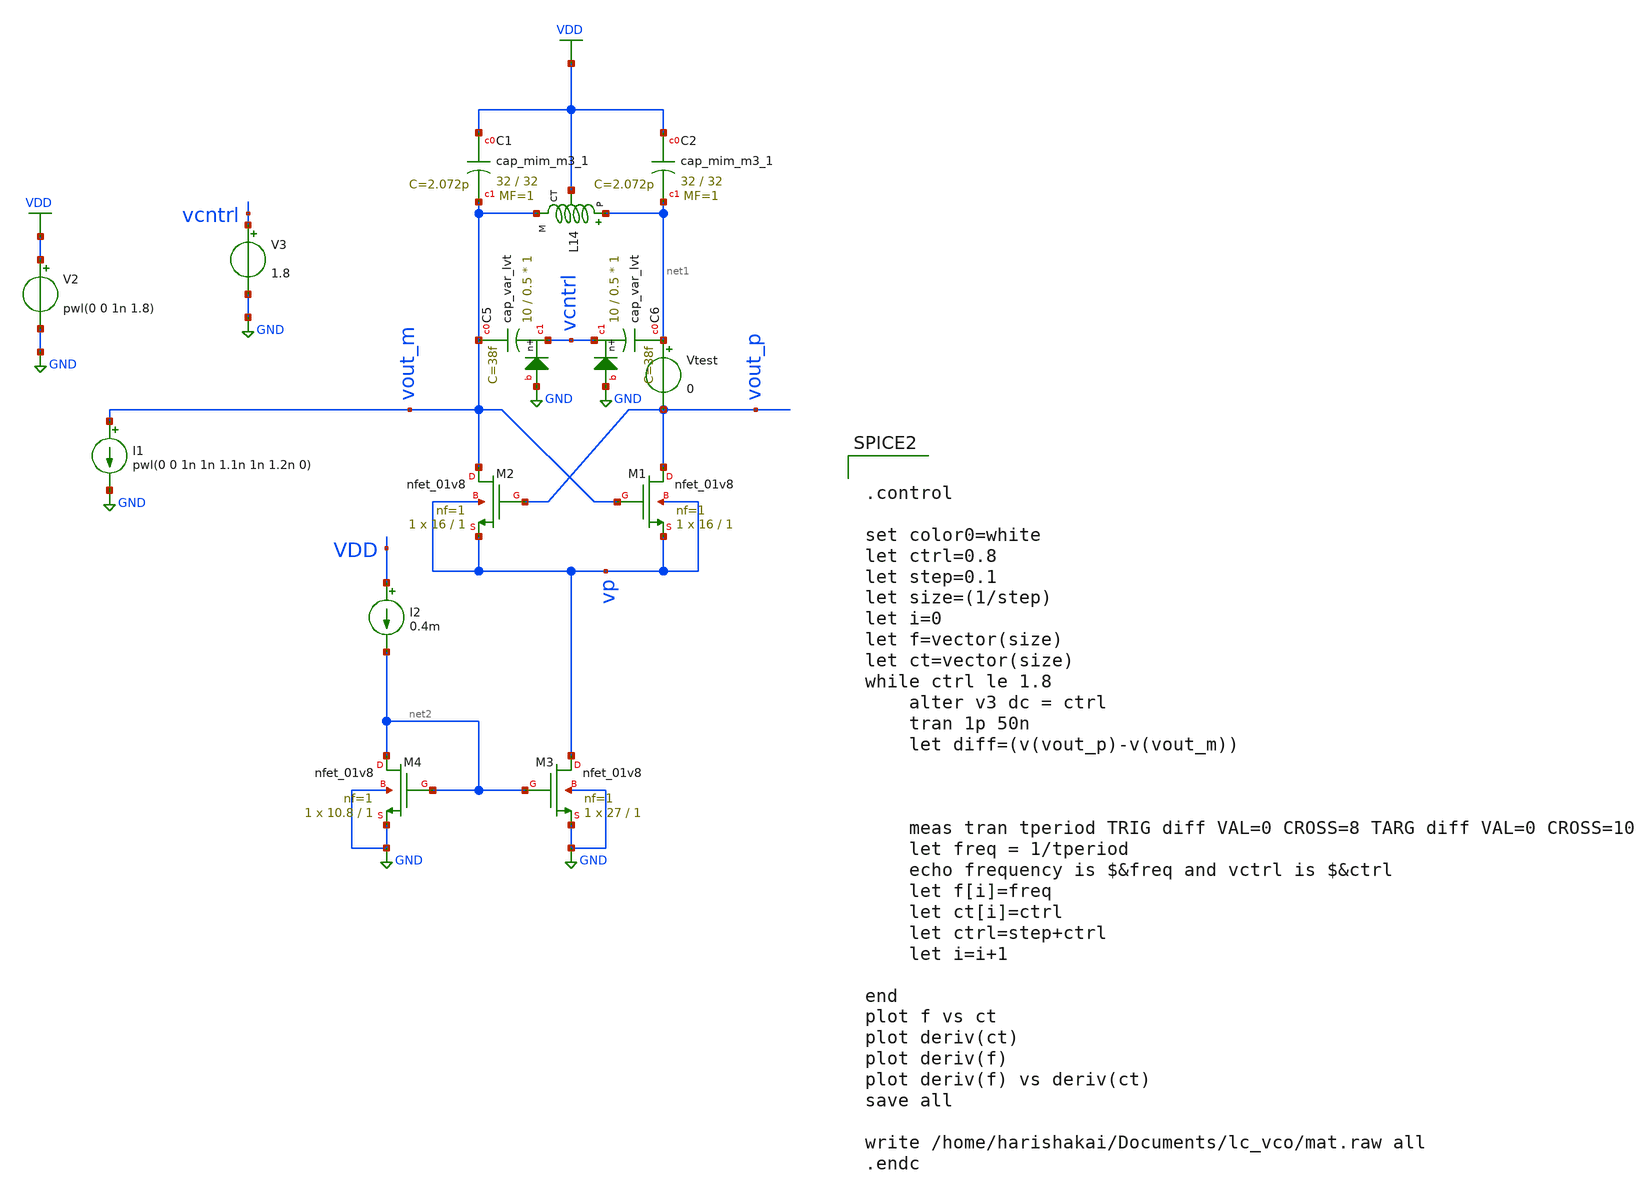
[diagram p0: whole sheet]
** sch_path: vco_cs_k.sch
**.subckt vco_cs_k
V2 VDD GND pwl(0 0 1n 1.8)
XC5 vout_m vcntrl GND sky130_fd_pr__cap_var_lvt W=10 L=0.5 VM=1 m=1
XC6 net1 vcntrl GND sky130_fd_pr__cap_var_lvt W=10 L=0.5 VM=1 m=1
I1 vout_m GND pwl(0 0 1n 1n 1.1n 1n 1.2n 0)
XM1 vout_p vout_m vp vp sky130_fd_pr__nfet_01v8 L=1 W=16 nf=1 ad='int((nf+1)/2) * W/nf * 0.29' as='int((nf+2)/2) * W/nf * 0.29'
+ pd='2*int((nf+1)/2) * (W/nf + 0.29)' ps='2*int((nf+2)/2) * (W/nf + 0.29)' nrd='0.29 / W' nrs='0.29 / W'
+ sa=0 sb=0 sd=0 mult=1 m=1
XM2 vout_m vout_p vp vp sky130_fd_pr__nfet_01v8 L=1 W=16 nf=1 ad='int((nf+1)/2) * W/nf * 0.29' as='int((nf+2)/2) * W/nf * 0.29'
+ pd='2*int((nf+1)/2) * (W/nf + 0.29)' ps='2*int((nf+2)/2) * (W/nf + 0.29)' nrd='0.29 / W' nrs='0.29 / W'
+ sa=0 sb=0 sd=0 mult=1 m=1
XC1 VDD vout_m sky130_fd_pr__cap_mim_m3_1 W=32 L=32 MF=1 m=1
XC2 VDD net1 sky130_fd_pr__cap_mim_m3_1 W=32 L=32 MF=1 m=1
XL14 net1 vout_m VDD GND sky130_fd_pr__ind_05_220
Vtest net1 vout_p 0
XM3 vp net2 GND GND sky130_fd_pr__nfet_01v8 L=1 W=27 nf=1 ad='int((nf+1)/2) * W/nf * 0.29' as='int((nf+2)/2) * W/nf * 0.29'
+ pd='2*int((nf+1)/2) * (W/nf + 0.29)' ps='2*int((nf+2)/2) * (W/nf + 0.29)' nrd='0.29 / W' nrs='0.29 / W'
+ sa=0 sb=0 sd=0 mult=1 m=1
XM4 net2 net2 GND GND sky130_fd_pr__nfet_01v8 L=1 W=10.8 nf=1 ad='int((nf+1)/2) * W/nf * 0.29' as='int((nf+2)/2) * W/nf * 0.29'
+ pd='2*int((nf+1)/2) * (W/nf + 0.29)' ps='2*int((nf+2)/2) * (W/nf + 0.29)' nrd='0.29 / W' nrs='0.29 / W'
+ sa=0 sb=0 sd=0 mult=1 m=1
I2 VDD net2 0.4m
V3 vcntrl GND 1.8
**** begin user architecture code


.option wnflag = 1
.lib /usr/local/share/pdk/sky130A/libs.tech/ngspice/sky130.lib.spice tt
.include /usr/local/share/pdk/sky130A/libs.ref/sky130_fd_pr/spice/sky130_fd_pr__ind_05_220.model.spice
.param mc_mm_switch=0




.control

set color0=white
let ctrl=0.8
let step=0.1
let size=(1/step)
let i=0
let f=vector(size)
let ct=vector(size)
while ctrl le 1.8
	alter v3 dc = ctrl
	tran 1p 50n
	let diff=(v(vout_p)-v(vout_m))



	meas tran tperiod TRIG diff VAL=0 CROSS=8 TARG diff VAL=0 CROSS=10
	let freq = 1/tperiod
	echo frequency is $&freq and vctrl is $&ctrl
	let f[i]=freq
	let ct[i]=ctrl
	let ctrl=step+ctrl
	let i=i+1

end
plot f vs ct
plot deriv(ct)
plot deriv(f)
plot deriv(f) vs deriv(ct)
save all

write /home/harishakai/Documents/lc_vco/mat.raw all
.endc


**** end user architecture code
**.ends
.GLOBAL VDD
.GLOBAL GND
.end
